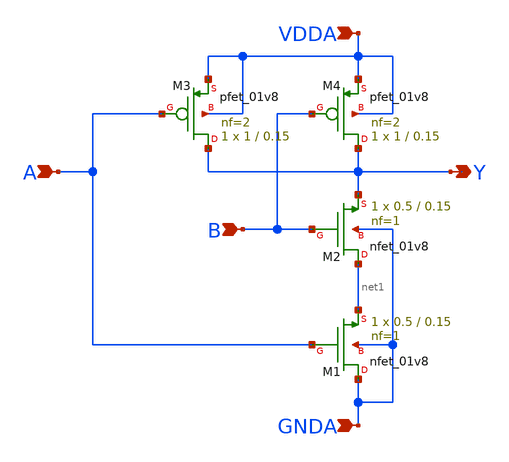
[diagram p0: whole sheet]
** sch_path: projects/pll/pfd/xschem_ngspice/nand_pfd.sch
**.subckt nand_pfd A Y VDDA GNDA B
*.ipin A
*.opin Y
*.ipin VDDA
*.ipin GNDA
*.ipin B
XM4 Y B VDDA VDDA sky130_fd_pr__pfet_01v8 L=0.15 W=1 nf=2 ad='int((nf+1)/2) * W/nf * 0.29' as='int((nf+2)/2) * W/nf * 0.29'
+ pd='2*int((nf+1)/2) * (W/nf + 0.29)' ps='2*int((nf+2)/2) * (W/nf + 0.29)' nrd='0.29 / W' nrs='0.29 / W'
+ sa=0 sb=0 sd=0 mult=1 m=1
XM2 net1 B Y GNDA sky130_fd_pr__nfet_01v8 L=0.15 W=0.5 nf=1 ad='int((nf+1)/2) * W/nf * 0.29' as='int((nf+2)/2) * W/nf * 0.29'
+ pd='2*int((nf+1)/2) * (W/nf + 0.29)' ps='2*int((nf+2)/2) * (W/nf + 0.29)' nrd='0.29 / W' nrs='0.29 / W'
+ sa=0 sb=0 sd=0 mult=1 m=1
XM1 GNDA A net1 GNDA sky130_fd_pr__nfet_01v8 L=0.15 W=0.5 nf=1 ad='int((nf+1)/2) * W/nf * 0.29' as='int((nf+2)/2) * W/nf * 0.29'
+ pd='2*int((nf+1)/2) * (W/nf + 0.29)' ps='2*int((nf+2)/2) * (W/nf + 0.29)' nrd='0.29 / W' nrs='0.29 / W'
+ sa=0 sb=0 sd=0 mult=1 m=1
XM3 Y A VDDA VDDA sky130_fd_pr__pfet_01v8 L=0.15 W=1 nf=2 ad='int((nf+1)/2) * W/nf * 0.29' as='int((nf+2)/2) * W/nf * 0.29'
+ pd='2*int((nf+1)/2) * (W/nf + 0.29)' ps='2*int((nf+2)/2) * (W/nf + 0.29)' nrd='0.29 / W' nrs='0.29 / W'
+ sa=0 sb=0 sd=0 mult=1 m=1
**.ends
.end
